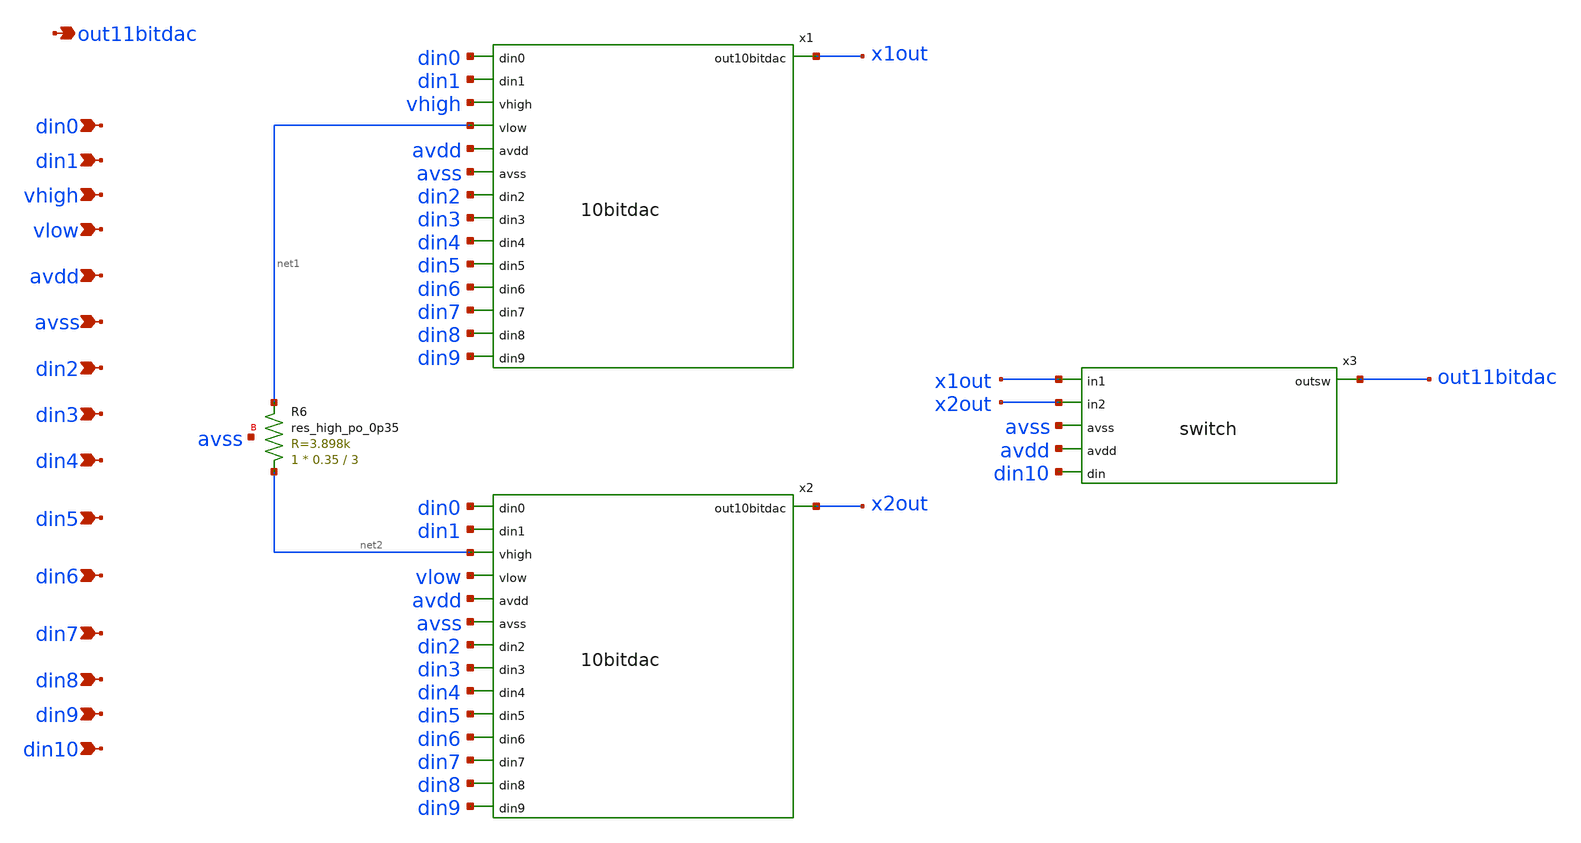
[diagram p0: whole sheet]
** sch_path: xschem/11bitdac.sch
**.subckt 11bitdac din0 din1 vhigh vlow avdd avss din2 din3 out11bitdac din4 din5 din6 din7 din8
*+ din9 din10
*.ipin din0
*.ipin din1
*.ipin vhigh
*.ipin vlow
*.ipin avdd
*.ipin avss
*.ipin din2
*.ipin din3
*.opin out11bitdac
*.ipin din4
*.ipin din5
*.ipin din6
*.ipin din7
*.ipin din8
*.ipin din9
*.ipin din10
x1 x1out din0 din1 vhigh net1 avdd avss din2 din3 din4 din5 din6 din7 din8 din9 10bitdac
x2 x2out din0 din1 net2 vlow avdd avss din2 din3 din4 din5 din6 din7 din8 din9 10bitdac
x3 out11bitdac x1out x2out avss avdd din10 switch
XR6 net2 net1 avss sky130_fd_pr__res_high_po_0p35 L=3 mult=1 m=1
**.ends
.end
